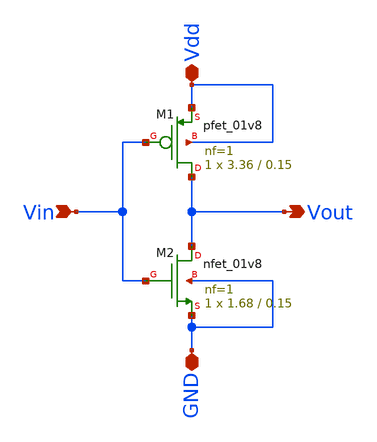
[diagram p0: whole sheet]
** sch_path: xschem_project/inv_x4/inv_x4.sch
**.subckt inv_x4 Vin Vout Vdd GND
*.ipin Vin
*.opin Vout
*.iopin Vdd
*.iopin GND
XM1 Vout Vin Vdd Vdd sky130_fd_pr__pfet_01v8 L=0.15 W=3.36 nf=1 ad='int((1 + 1)/2) * 3.36 / 1 * 0.29'
+ as='int((1 + 2)/2) * 3.36 / 1 * 0.29' pd='2*int((1 + 1)/2) * (3.36 / 1 + 0.29)' ps='2*int((1 + 2)/2) * (3.36 / 1 + 0.29)'
+ nrd='0.29 / 3.36 ' nrs='0.29 / 3.36 ' sa=0 sb=0 sd=0 mult=1 m=1
XM2 Vout Vin GND GND sky130_fd_pr__nfet_01v8 L=0.15 W=1.68 nf=1 ad='int((1 + 1)/2) * 1.68 / 1 * 0.29'
+ as='int((1 + 2)/2) * 1.68 / 1 * 0.29' pd='2*int((1 + 1)/2) * (1.68 / 1 + 0.29)' ps='2*int((1 + 2)/2) * (1.68 / 1 + 0.29)'
+ nrd='0.29 / 1.68 ' nrs='0.29 / 1.68 ' sa=0 sb=0 sd=0 mult=1 m=1
**.ends
.end
